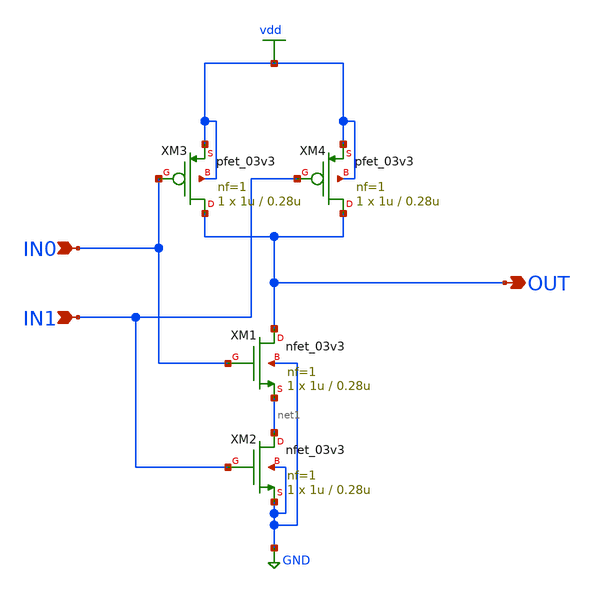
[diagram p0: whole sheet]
** sch_path: schematics/add/NAND2.sch
**.subckt NAND2 OUT IN0 IN1
*.opin OUT
*.ipin IN0
*.ipin IN1
XM1 OUT IN0 net1 GND nfet_03v3 L=0.28u W=1u nf=1 ad='int((nf+1)/2) * W/nf * 0.18u' as='int((nf+2)/2) * W/nf * 0.18u'
+ pd='2*int((nf+1)/2) * (W/nf + 0.18u)' ps='2*int((nf+2)/2) * (W/nf + 0.18u)' nrd='0.18u / W' nrs='0.18u / W'
+ sa=0 sb=0 sd=0 m=1
XM2 net1 IN1 GND GND nfet_03v3 L=0.28u W=1u nf=1 ad='int((nf+1)/2) * W/nf * 0.18u' as='int((nf+2)/2) * W/nf * 0.18u'
+ pd='2*int((nf+1)/2) * (W/nf + 0.18u)' ps='2*int((nf+2)/2) * (W/nf + 0.18u)' nrd='0.18u / W' nrs='0.18u / W'
+ sa=0 sb=0 sd=0 m=1
XM3 OUT IN0 vdd vdd pfet_03v3 L=0.28u W=1u nf=1 ad='int((nf+1)/2) * W/nf * 0.18u' as='int((nf+2)/2) * W/nf * 0.18u'
+ pd='2*int((nf+1)/2) * (W/nf + 0.18u)' ps='2*int((nf+2)/2) * (W/nf + 0.18u)' nrd='0.18u / W' nrs='0.18u / W'
+ sa=0 sb=0 sd=0 m=1
XM4 OUT IN1 vdd vdd pfet_03v3 L=0.28u W=1u nf=1 ad='int((nf+1)/2) * W/nf * 0.18u' as='int((nf+2)/2) * W/nf * 0.18u'
+ pd='2*int((nf+1)/2) * (W/nf + 0.18u)' ps='2*int((nf+2)/2) * (W/nf + 0.18u)' nrd='0.18u / W' nrs='0.18u / W'
+ sa=0 sb=0 sd=0 m=1
**.ends
.GLOBAL GND
.GLOBAL vdd
.end
